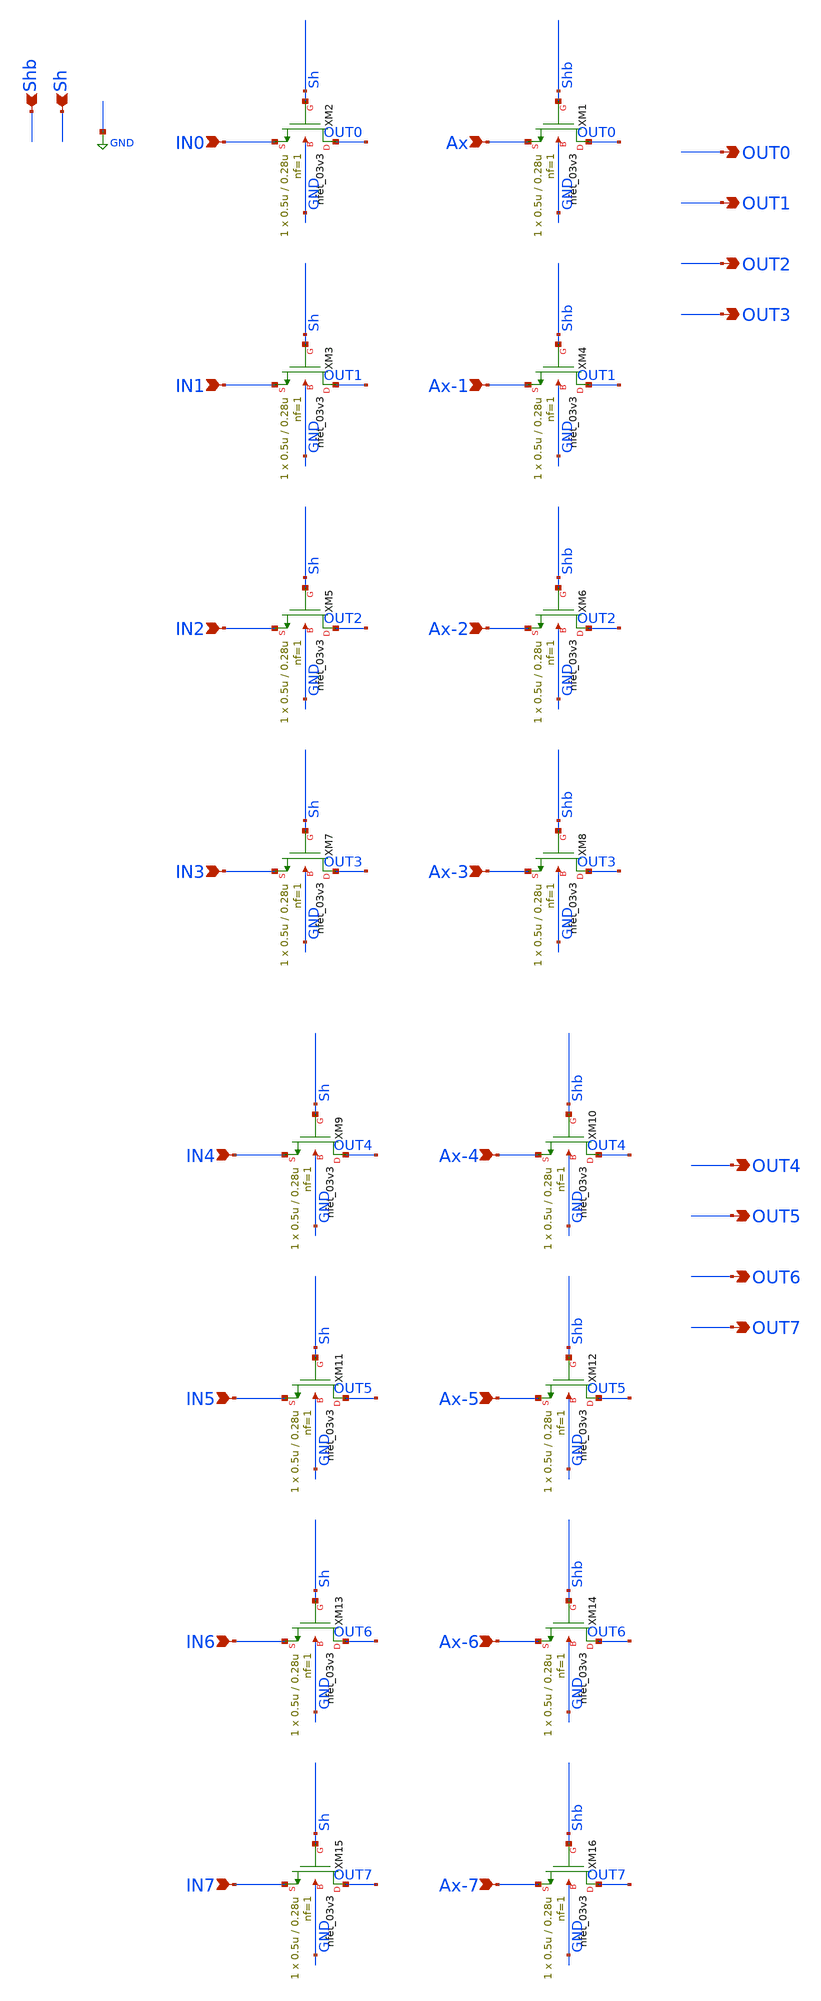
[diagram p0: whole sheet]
** sch_path: 8BIT.sch
**.subckt 8BIT Sh Shb OUT0 Ax IN0 Ax-1 IN1 OUT1 Ax-2 IN2 Ax-3 IN3 OUT2 OUT3 OUT4 Ax-4 IN4 Ax-5 IN5
*+ OUT5 Ax-6 IN6 Ax-7 IN7 OUT6 OUT7
*.ipin Sh
*.ipin Shb
*.opin OUT0
*.ipin Ax
*.ipin IN0
*.ipin Ax-1
*.ipin IN1
*.opin OUT1
*.ipin Ax-2
*.ipin IN2
*.ipin Ax-3
*.ipin IN3
*.opin OUT2
*.opin OUT3
*.opin OUT4
*.ipin Ax-4
*.ipin IN4
*.ipin Ax-5
*.ipin IN5
*.opin OUT5
*.ipin Ax-6
*.ipin IN6
*.ipin Ax-7
*.ipin IN7
*.opin OUT6
*.opin OUT7
XM2 OUT0 Sh IN0 GND nfet_03v3 L=0.28u W=0.5u nf=1 ad='int((nf+1)/2) * W/nf * 0.18u' as='int((nf+2)/2) * W/nf * 0.18u'
+ pd='2*int((nf+1)/2) * (W/nf + 0.18u)' ps='2*int((nf+2)/2) * (W/nf + 0.18u)' nrd='0.18u / W' nrs='0.18u / W'
+ sa=0 sb=0 sd=0 m=1
XM1 OUT0 Shb Ax GND nfet_03v3 L=0.28u W=0.5u nf=1 ad='int((nf+1)/2) * W/nf * 0.18u' as='int((nf+2)/2) * W/nf * 0.18u'
+ pd='2*int((nf+1)/2) * (W/nf + 0.18u)' ps='2*int((nf+2)/2) * (W/nf + 0.18u)' nrd='0.18u / W' nrs='0.18u / W'
+ sa=0 sb=0 sd=0 m=1
XM3 OUT1 Sh IN1 GND nfet_03v3 L=0.28u W=0.5u nf=1 ad='int((nf+1)/2) * W/nf * 0.18u' as='int((nf+2)/2) * W/nf * 0.18u'
+ pd='2*int((nf+1)/2) * (W/nf + 0.18u)' ps='2*int((nf+2)/2) * (W/nf + 0.18u)' nrd='0.18u / W' nrs='0.18u / W'
+ sa=0 sb=0 sd=0 m=1
XM4 OUT1 Shb Ax-1 GND nfet_03v3 L=0.28u W=0.5u nf=1 ad='int((nf+1)/2) * W/nf * 0.18u' as='int((nf+2)/2) * W/nf * 0.18u'
+ pd='2*int((nf+1)/2) * (W/nf + 0.18u)' ps='2*int((nf+2)/2) * (W/nf + 0.18u)' nrd='0.18u / W' nrs='0.18u / W'
+ sa=0 sb=0 sd=0 m=1
XM5 OUT2 Sh IN2 GND nfet_03v3 L=0.28u W=0.5u nf=1 ad='int((nf+1)/2) * W/nf * 0.18u' as='int((nf+2)/2) * W/nf * 0.18u'
+ pd='2*int((nf+1)/2) * (W/nf + 0.18u)' ps='2*int((nf+2)/2) * (W/nf + 0.18u)' nrd='0.18u / W' nrs='0.18u / W'
+ sa=0 sb=0 sd=0 m=1
XM6 OUT2 Shb Ax-2 GND nfet_03v3 L=0.28u W=0.5u nf=1 ad='int((nf+1)/2) * W/nf * 0.18u' as='int((nf+2)/2) * W/nf * 0.18u'
+ pd='2*int((nf+1)/2) * (W/nf + 0.18u)' ps='2*int((nf+2)/2) * (W/nf + 0.18u)' nrd='0.18u / W' nrs='0.18u / W'
+ sa=0 sb=0 sd=0 m=1
XM7 OUT3 Sh IN3 GND nfet_03v3 L=0.28u W=0.5u nf=1 ad='int((nf+1)/2) * W/nf * 0.18u' as='int((nf+2)/2) * W/nf * 0.18u'
+ pd='2*int((nf+1)/2) * (W/nf + 0.18u)' ps='2*int((nf+2)/2) * (W/nf + 0.18u)' nrd='0.18u / W' nrs='0.18u / W'
+ sa=0 sb=0 sd=0 m=1
XM8 OUT3 Shb Ax-3 GND nfet_03v3 L=0.28u W=0.5u nf=1 ad='int((nf+1)/2) * W/nf * 0.18u' as='int((nf+2)/2) * W/nf * 0.18u'
+ pd='2*int((nf+1)/2) * (W/nf + 0.18u)' ps='2*int((nf+2)/2) * (W/nf + 0.18u)' nrd='0.18u / W' nrs='0.18u / W'
+ sa=0 sb=0 sd=0 m=1
XM9 OUT4 Sh IN4 GND nfet_03v3 L=0.28u W=0.5u nf=1 ad='int((nf+1)/2) * W/nf * 0.18u' as='int((nf+2)/2) * W/nf * 0.18u'
+ pd='2*int((nf+1)/2) * (W/nf + 0.18u)' ps='2*int((nf+2)/2) * (W/nf + 0.18u)' nrd='0.18u / W' nrs='0.18u / W'
+ sa=0 sb=0 sd=0 m=1
XM10 OUT4 Shb Ax-4 GND nfet_03v3 L=0.28u W=0.5u nf=1 ad='int((nf+1)/2) * W/nf * 0.18u' as='int((nf+2)/2) * W/nf * 0.18u'
+ pd='2*int((nf+1)/2) * (W/nf + 0.18u)' ps='2*int((nf+2)/2) * (W/nf + 0.18u)' nrd='0.18u / W' nrs='0.18u / W'
+ sa=0 sb=0 sd=0 m=1
XM11 OUT5 Sh IN5 GND nfet_03v3 L=0.28u W=0.5u nf=1 ad='int((nf+1)/2) * W/nf * 0.18u' as='int((nf+2)/2) * W/nf * 0.18u'
+ pd='2*int((nf+1)/2) * (W/nf + 0.18u)' ps='2*int((nf+2)/2) * (W/nf + 0.18u)' nrd='0.18u / W' nrs='0.18u / W'
+ sa=0 sb=0 sd=0 m=1
XM12 OUT5 Shb Ax-5 GND nfet_03v3 L=0.28u W=0.5u nf=1 ad='int((nf+1)/2) * W/nf * 0.18u' as='int((nf+2)/2) * W/nf * 0.18u'
+ pd='2*int((nf+1)/2) * (W/nf + 0.18u)' ps='2*int((nf+2)/2) * (W/nf + 0.18u)' nrd='0.18u / W' nrs='0.18u / W'
+ sa=0 sb=0 sd=0 m=1
XM13 OUT6 Sh IN6 GND nfet_03v3 L=0.28u W=0.5u nf=1 ad='int((nf+1)/2) * W/nf * 0.18u' as='int((nf+2)/2) * W/nf * 0.18u'
+ pd='2*int((nf+1)/2) * (W/nf + 0.18u)' ps='2*int((nf+2)/2) * (W/nf + 0.18u)' nrd='0.18u / W' nrs='0.18u / W'
+ sa=0 sb=0 sd=0 m=1
XM14 OUT6 Shb Ax-6 GND nfet_03v3 L=0.28u W=0.5u nf=1 ad='int((nf+1)/2) * W/nf * 0.18u' as='int((nf+2)/2) * W/nf * 0.18u'
+ pd='2*int((nf+1)/2) * (W/nf + 0.18u)' ps='2*int((nf+2)/2) * (W/nf + 0.18u)' nrd='0.18u / W' nrs='0.18u / W'
+ sa=0 sb=0 sd=0 m=1
XM15 OUT7 Sh IN7 GND nfet_03v3 L=0.28u W=0.5u nf=1 ad='int((nf+1)/2) * W/nf * 0.18u' as='int((nf+2)/2) * W/nf * 0.18u'
+ pd='2*int((nf+1)/2) * (W/nf + 0.18u)' ps='2*int((nf+2)/2) * (W/nf + 0.18u)' nrd='0.18u / W' nrs='0.18u / W'
+ sa=0 sb=0 sd=0 m=1
XM16 OUT7 Shb Ax-7 GND nfet_03v3 L=0.28u W=0.5u nf=1 ad='int((nf+1)/2) * W/nf * 0.18u' as='int((nf+2)/2) * W/nf * 0.18u'
+ pd='2*int((nf+1)/2) * (W/nf + 0.18u)' ps='2*int((nf+2)/2) * (W/nf + 0.18u)' nrd='0.18u / W' nrs='0.18u / W'
+ sa=0 sb=0 sd=0 m=1
**.ends
.GLOBAL GND
.end
